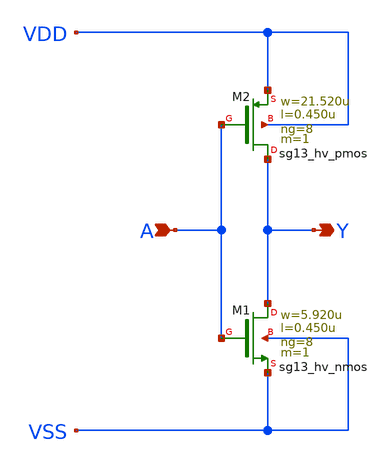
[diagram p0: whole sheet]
** sch_path: ihp-sg13g2/libs.ref/sg13g2_stdcell_hv/sch/xschem/sg13g2_hv_inv_8.sch
* Copyright 2023 IHP PDK Authors
* Licensed under the Apache License, Version 2.0 (the "License");
* you may not use this file except in compliance with the License.
* You may obtain a copy of the License at
* https://www.apache.org/licenses/LICENSE-2.0
* Unless required by applicable law or agreed to in writing, software
* distributed under the License is distributed on an "AS IS" BASIS,
* WITHOUT WARRANTIES OR CONDITIONS OF ANY KIND, either express or implied.
* See the License for the specific language governing permissions and
* limitations under the License.
**.subckt sg13g2_hv_inv_8 Y A
*.opin Y
*.ipin A
XM1 Y A VSS VSS sg13_hv_nmos w=5.920u l=0.450u ng=8 m=1 mm_ok=1
XM2 Y A VDD VDD sg13_hv_pmos w=21.520u l=0.450u ng=8 m=1 mm_ok=1
**.ends
.end
